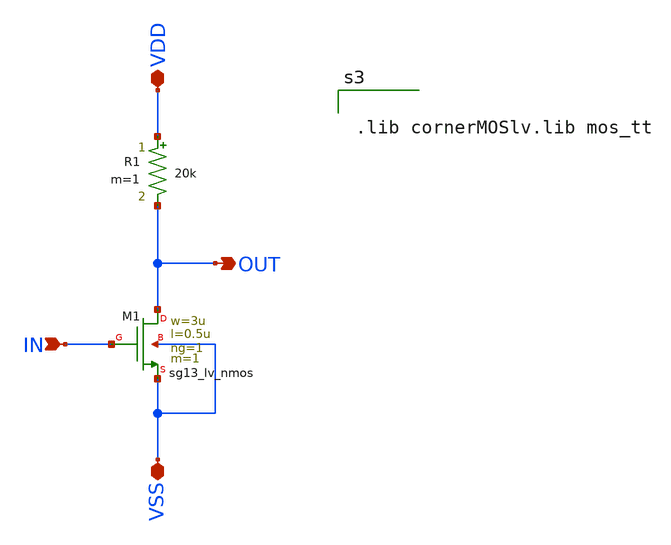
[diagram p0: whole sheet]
** sch_path: BTDay3-Ex/CS_Amplifier_R.sch
**.subckt CS_Amplifier_R IN VSS VDD OUT
*.ipin IN
*.iopin VSS
*.iopin VDD
*.opin OUT
XM1 OUT IN VSS VSS sg13_lv_nmos w=3u l=0.5u ng=1 m=1 mm_ok=1
R1 VDD OUT 20k m=1
**** begin user architecture code


.lib cornerMOSlv.lib mos_tt


**** end user architecture code
**.ends
.end
